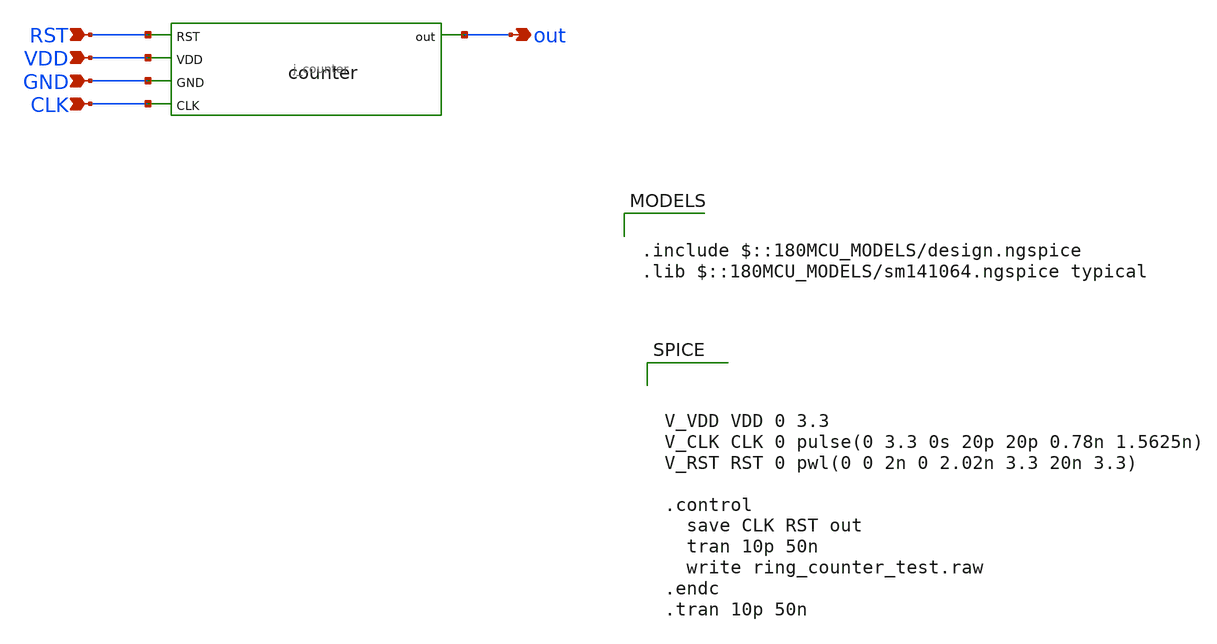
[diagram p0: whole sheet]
** sch_path: blocks/dsp-fft/tb/j_counter_tb.sch
**.subckt j_counter_tb VDD RST GND CLK out
*.ipin VDD
*.ipin RST
*.ipin GND
*.ipin CLK
*.opin out
x1 out RST VDD GND CLK j_counter
**** begin user architecture code

.include $::180MCU_MODELS/design.ngspice
.lib $::180MCU_MODELS/sm141064.ngspice typical




V_VDD VDD 0 3.3
V_CLK CLK 0 pulse(0 3.3 0s 20p 20p 0.78n 1.5625n)
V_RST RST 0 pwl(0 0 2n 0 2.02n 3.3 20n 3.3)

.control
  save CLK RST out
  tran 10p 50n
  write ring_counter_test.raw
.endc
.tran 10p 50n



**** end user architecture code
**.ends
.end
